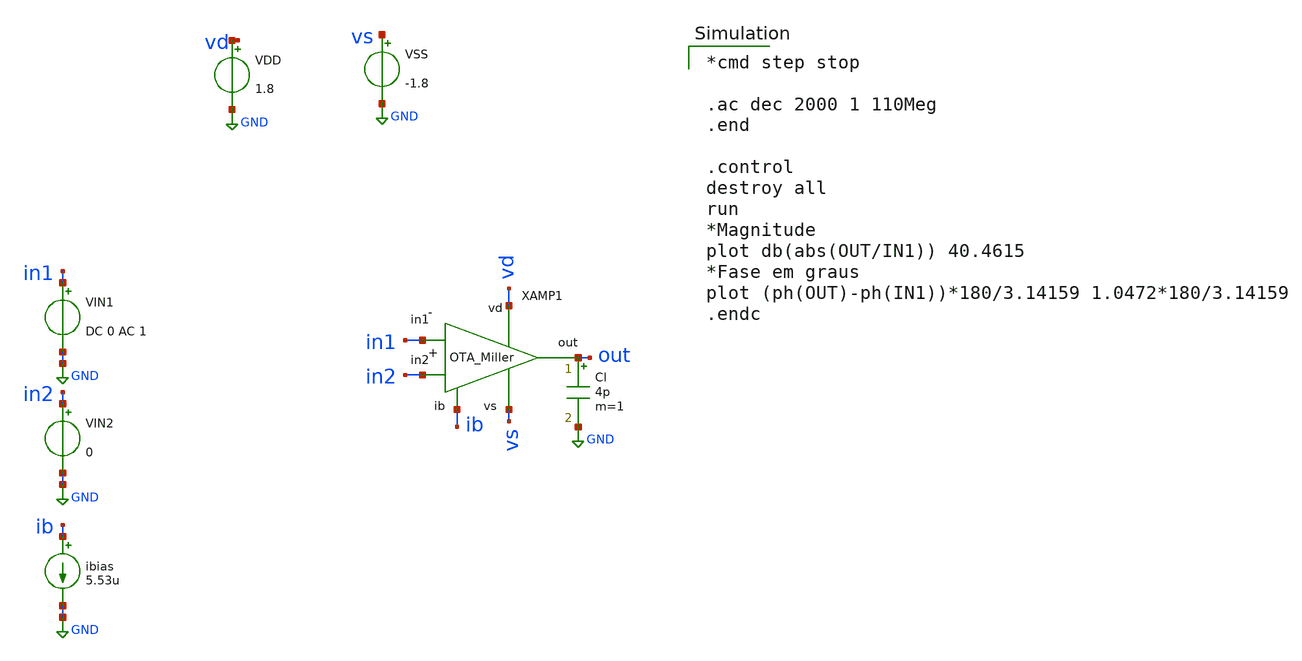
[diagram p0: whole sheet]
** sch_path: xschem/ota_tb-ac.sch
* Copyright 2020 Stefan Frederik Schippers
* Licensed under the Apache License, Version 2.0 (the "License");
* you may not use this file except in compliance with the License.
* You may obtain a copy of the License at
* https://www.apache.org/licenses/LICENSE-2.0
* Unless required by applicable law or agreed to in writing, software
* distributed under the License is distributed on an "AS IS" BASIS,
* WITHOUT WARRANTIES OR CONDITIONS OF ANY KIND, either express or implied.
* See the License for the specific language governing permissions and
* limitations under the License.
**.subckt ota_tb-ac
VIN2 in2 GND 0
VIN1 in1 GND DC 0 AC 1
ibias ib GND 5.53u
VDD net1 GND 1.8
VSS vs GND -1.8
X1 vd ib out in2 in1 vs ota
Cl out GND 4p m=1
**** begin user architecture code

*cmd step stop

.ac dec 2000 1 110Meg
.end

.control
destroy all
run
*Magnitude
plot db(abs(OUT/IN1)) 40.4615
*Fase em graus
plot (ph(OUT)-ph(IN1))*180/3.14159 1.0472*180/3.14159
.endc


.lib /home/hugodg/sky130_skel/dpga-ieee-sscs-contest-main/minimal_libs/skywater-pdk-libs-sky130_fd_pr/models/sky130.lib.spice tt
*.include /home/hugodg/sky130_skel/dpga-ieee-sscs-contest-main/minimal_libs/sky130_libs/sky130_lib.spice

**** end user architecture code
**.ends

* expanding   symbol:  /home/hugodg/sky130_skel/dpga-ieee-sscs-contest-main/xschem/ota.sym # of
*+ pins=6
** sym_path: xschem/ota.sym
** sch_path: xschem/ota.sch
.subckt ota vd ib out in2 in1 vs
*.iopin vd
*.iopin vs
*.iopin ib
*.ipin in1
*.ipin in2
*.opin out
XM4 d c vs vs sky130_fd_pr__nfet_01v8 L=1 W=0.861 nf=1 ad='int((nf+1)/2) * W/nf * 0.29' as='int((nf+2)/2) * W/nf * 0.29'
+ pd='2*int((nf+1)/2) * (W/nf + 0.29)' ps='2*int((nf+2)/2) * (W/nf + 0.29)' nrd='0.29 / W' nrs='0.29 / W'
+ sa=0 sb=0 sd=0 mult=1 m=1
XM7 e d vs vs sky130_fd_pr__nfet_01v8 L=1 W=8.61 nf=2 ad='int((nf+1)/2) * W/nf * 0.29' as='int((nf+2)/2) * W/nf * 0.29'
+ pd='2*int((nf+1)/2) * (W/nf + 0.29)' ps='2*int((nf+2)/2) * (W/nf + 0.29)' nrd='0.29 / W' nrs='0.29 / W'
+ sa=0 sb=0 sd=0 mult=1 m=1
XM5 ib ib vd vd sky130_fd_pr__pfet_01v8 L=1 W=5.85 nf=1 ad='int((nf+1)/2) * W/nf * 0.29' as='int((nf+2)/2) * W/nf * 0.29'
+ pd='2*int((nf+1)/2) * (W/nf + 0.29)' ps='2*int((nf+2)/2) * (W/nf + 0.29)' nrd='0.29 / W' nrs='0.29 / W'
+ sa=0 sb=0 sd=0 mult=1 m=1
XM6 b ib vd vd sky130_fd_pr__pfet_01v8 L=1 W=5.85 nf=1 ad='int((nf+1)/2) * W/nf * 0.29' as='int((nf+2)/2) * W/nf * 0.29'
+ pd='2*int((nf+1)/2) * (W/nf + 0.29)' ps='2*int((nf+2)/2) * (W/nf + 0.29)' nrd='0.29 / W' nrs='0.29 / W'
+ sa=0 sb=0 sd=0 mult=1 m=1
XM8 e ib vd vd sky130_fd_pr__pfet_01v8 L=1 W=29.3 nf=5 ad='int((nf+1)/2) * W/nf * 0.29' as='int((nf+2)/2) * W/nf * 0.29'
+ pd='2*int((nf+1)/2) * (W/nf + 0.29)' ps='2*int((nf+2)/2) * (W/nf + 0.29)' nrd='0.29 / W' nrs='0.29 / W'
+ sa=0 sb=0 sd=0 mult=1 m=1
XM10 out ib vd vd sky130_fd_pr__pfet_01v8 L=1 W=5.85 nf=1 ad='int((nf+1)/2) * W/nf * 0.29' as='int((nf+2)/2) * W/nf * 0.29'
+ pd='2*int((nf+1)/2) * (W/nf + 0.29)' ps='2*int((nf+2)/2) * (W/nf + 0.29)' nrd='0.29 / W' nrs='0.29 / W'
+ sa=0 sb=0 sd=0 mult=1 m=1
XM9 vs e out out sky130_fd_pr__pfet_01v8 L=1 W=5.85 nf=1 ad='int((nf+1)/2) * W/nf * 0.29' as='int((nf+2)/2) * W/nf * 0.29'
+ pd='2*int((nf+1)/2) * (W/nf + 0.29)' ps='2*int((nf+2)/2) * (W/nf + 0.29)' nrd='0.29 / W' nrs='0.29 / W'
+ sa=0 sb=0 sd=0 mult=1 m=1
XM1 c in1 b b sky130_fd_pr__pfet_01v8 L=1 W=2.93 nf=1 ad='int((nf+1)/2) * W/nf * 0.29' as='int((nf+2)/2) * W/nf * 0.29'
+ pd='2*int((nf+1)/2) * (W/nf + 0.29)' ps='2*int((nf+2)/2) * (W/nf + 0.29)' nrd='0.29 / W' nrs='0.29 / W'
+ sa=0 sb=0 sd=0 mult=1 m=1
XM2 d in2 b b sky130_fd_pr__pfet_01v8 L=1 W=2.93 nf=1 ad='int((nf+1)/2) * W/nf * 0.29' as='int((nf+2)/2) * W/nf * 0.29'
+ pd='2*int((nf+1)/2) * (W/nf + 0.29)' ps='2*int((nf+2)/2) * (W/nf + 0.29)' nrd='0.29 / W' nrs='0.29 / W'
+ sa=0 sb=0 sd=0 mult=1 m=1
XM3 c c vs vs sky130_fd_pr__nfet_01v8 L=1 W=0.861 nf=1 ad='int((nf+1)/2) * W/nf * 0.29' as='int((nf+2)/2) * W/nf * 0.29'
+ pd='2*int((nf+1)/2) * (W/nf + 0.29)' ps='2*int((nf+2)/2) * (W/nf + 0.29)' nrd='0.29 / W' nrs='0.29 / W'
+ sa=0 sb=0 sd=0 mult=1 m=1
XCC e d sky130_fd_pr__cap_mim_m3_1 W=22.023 L=22.023 MF=1 m=1
.ends

.GLOBAL GND
.end
